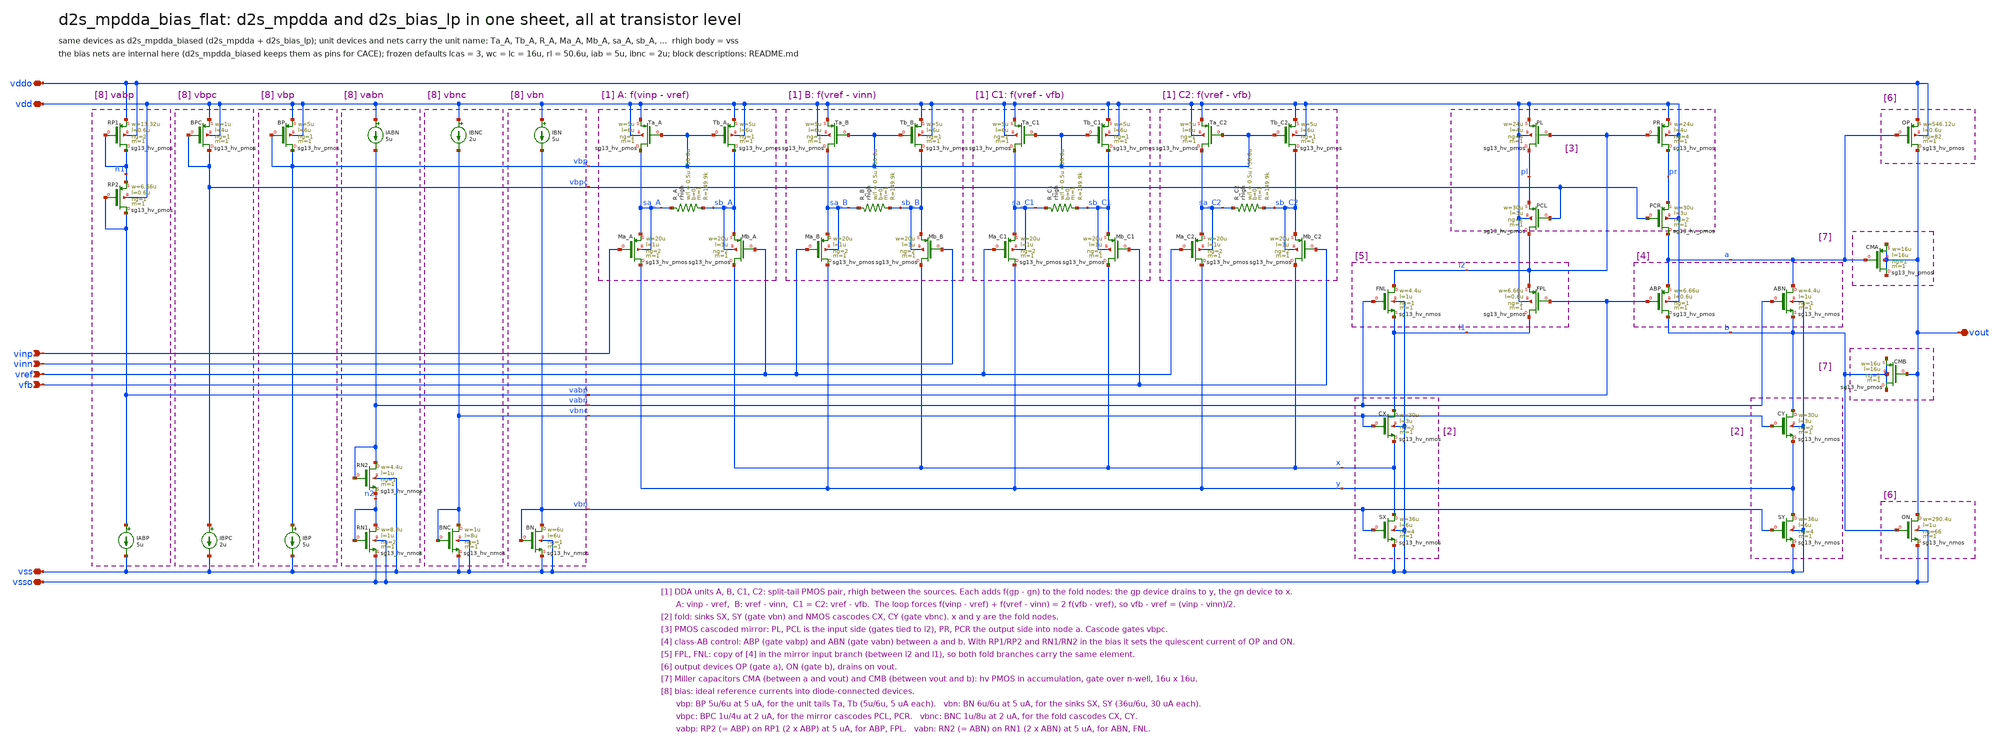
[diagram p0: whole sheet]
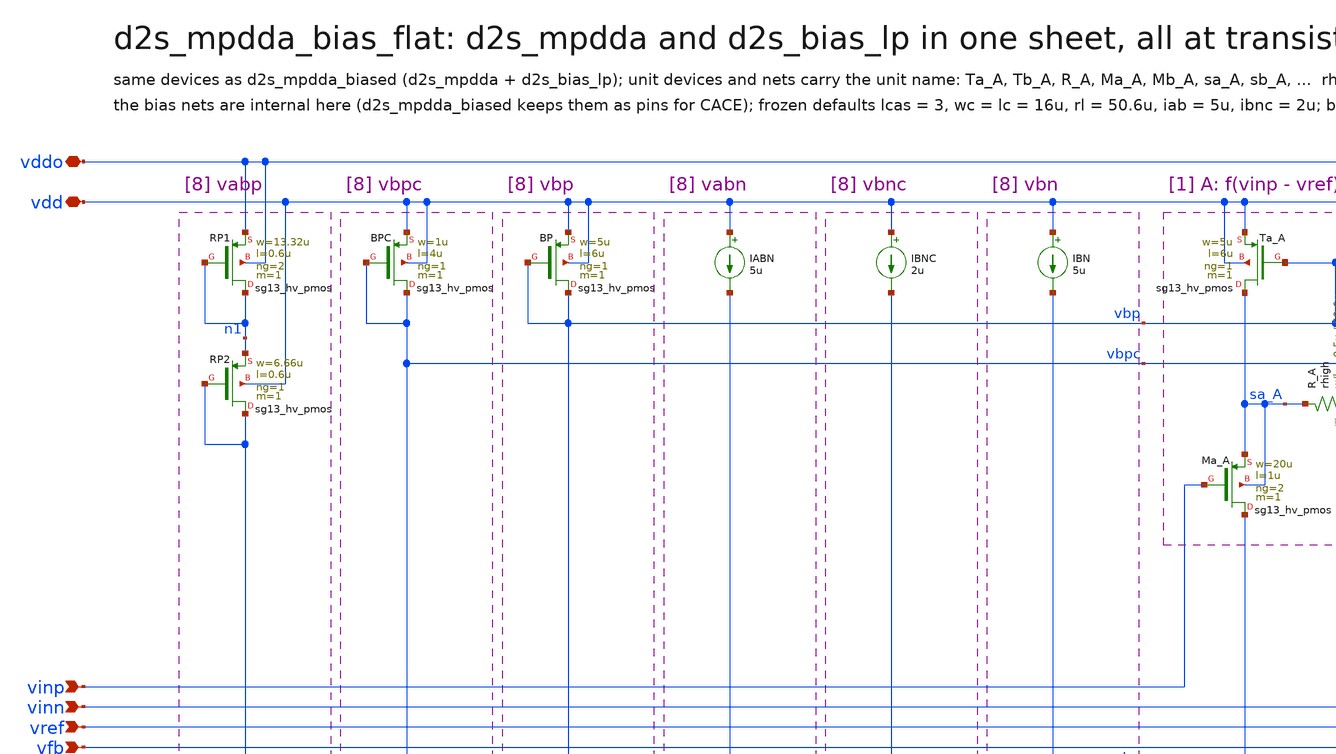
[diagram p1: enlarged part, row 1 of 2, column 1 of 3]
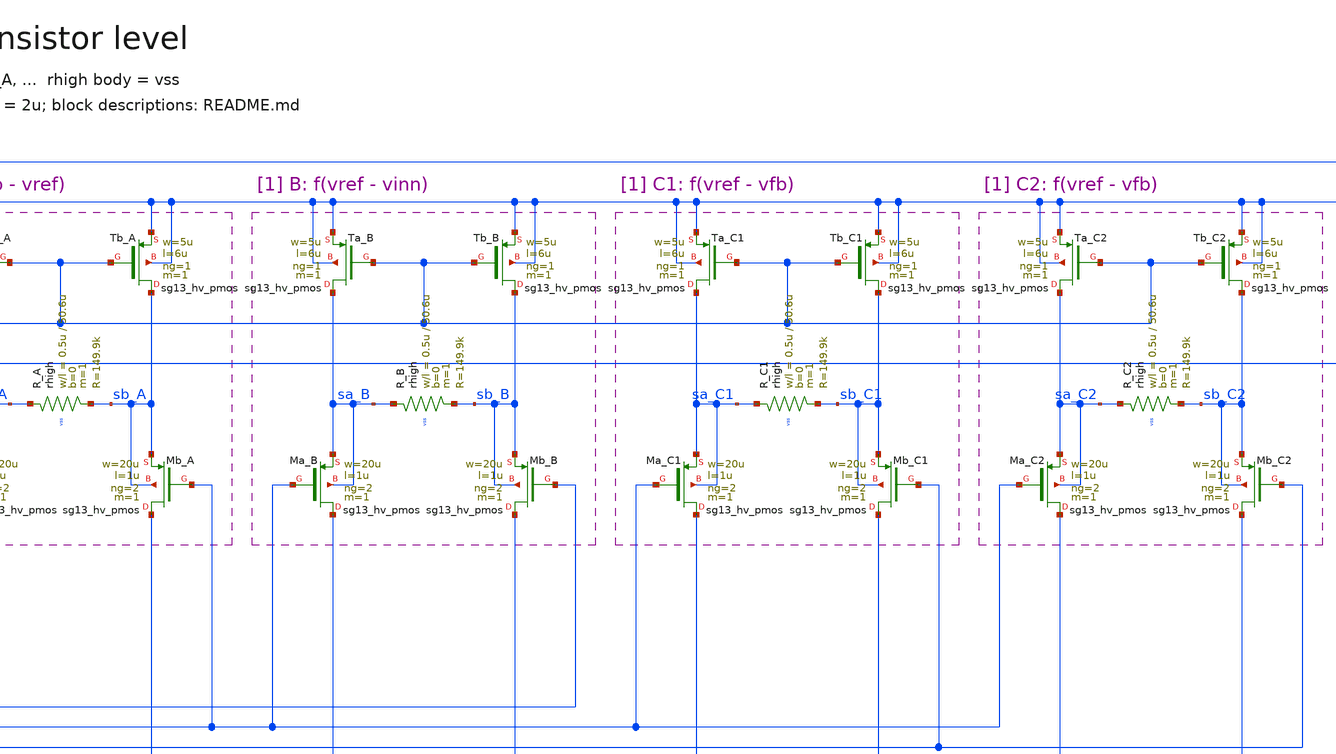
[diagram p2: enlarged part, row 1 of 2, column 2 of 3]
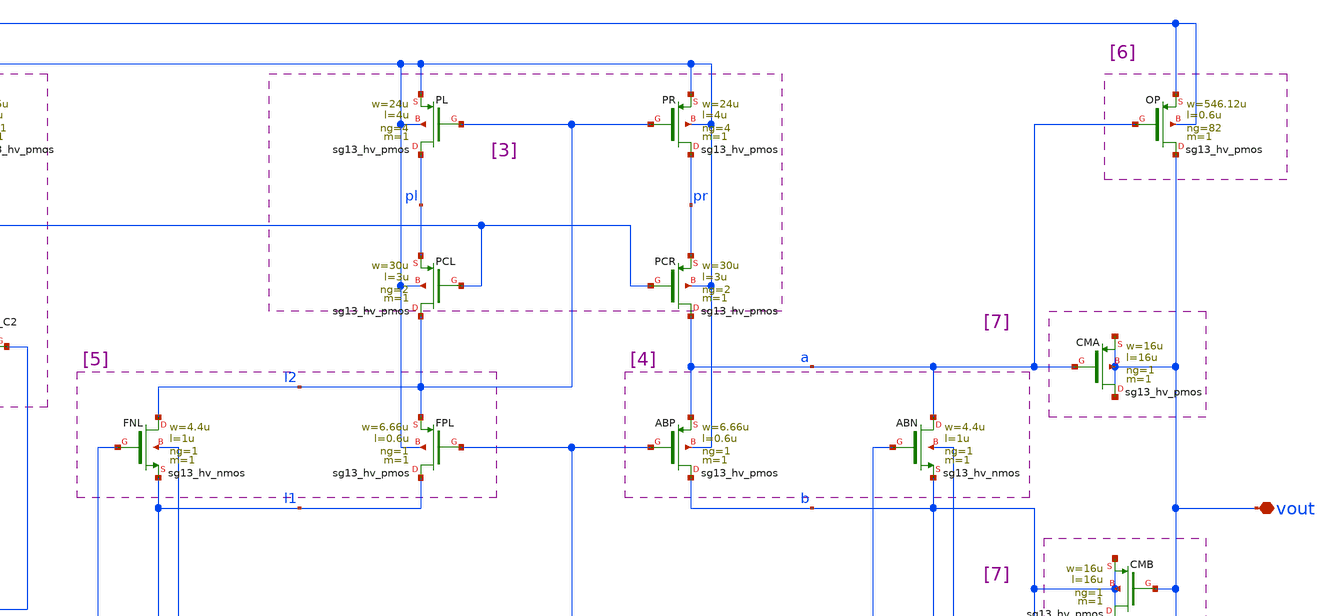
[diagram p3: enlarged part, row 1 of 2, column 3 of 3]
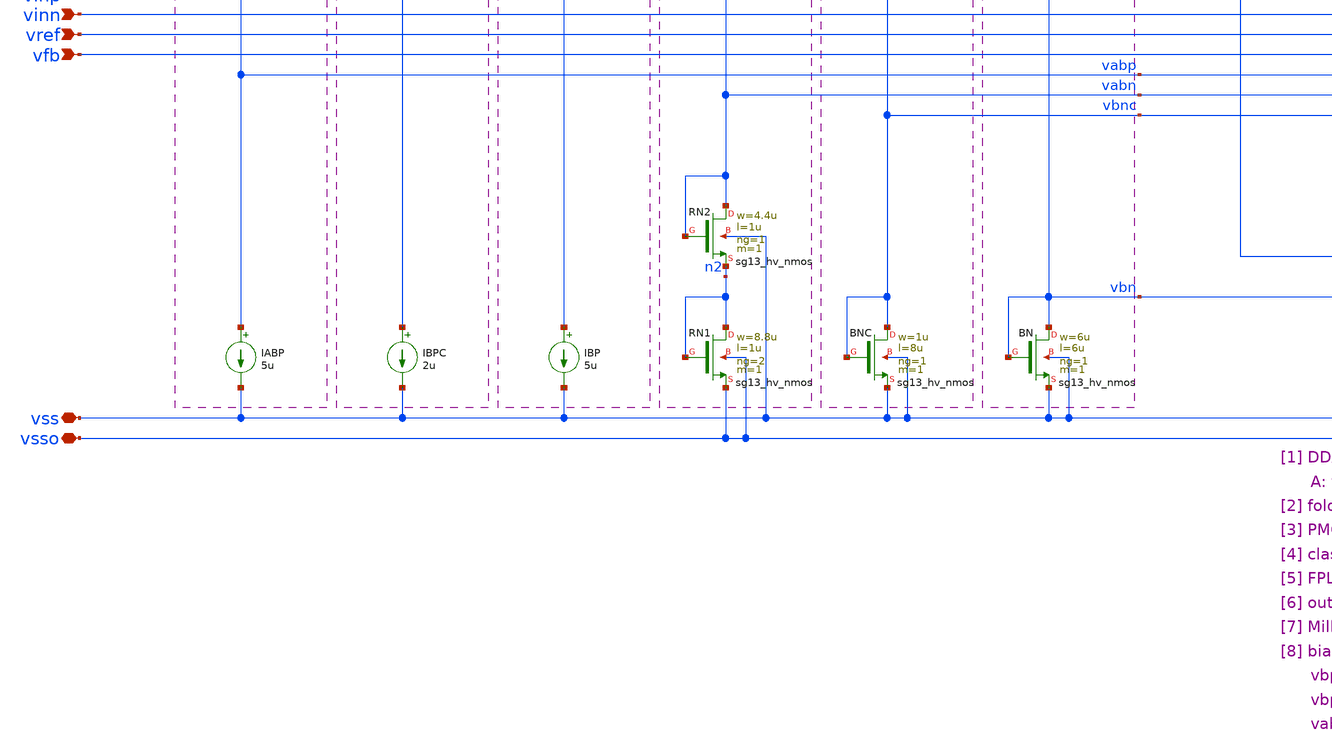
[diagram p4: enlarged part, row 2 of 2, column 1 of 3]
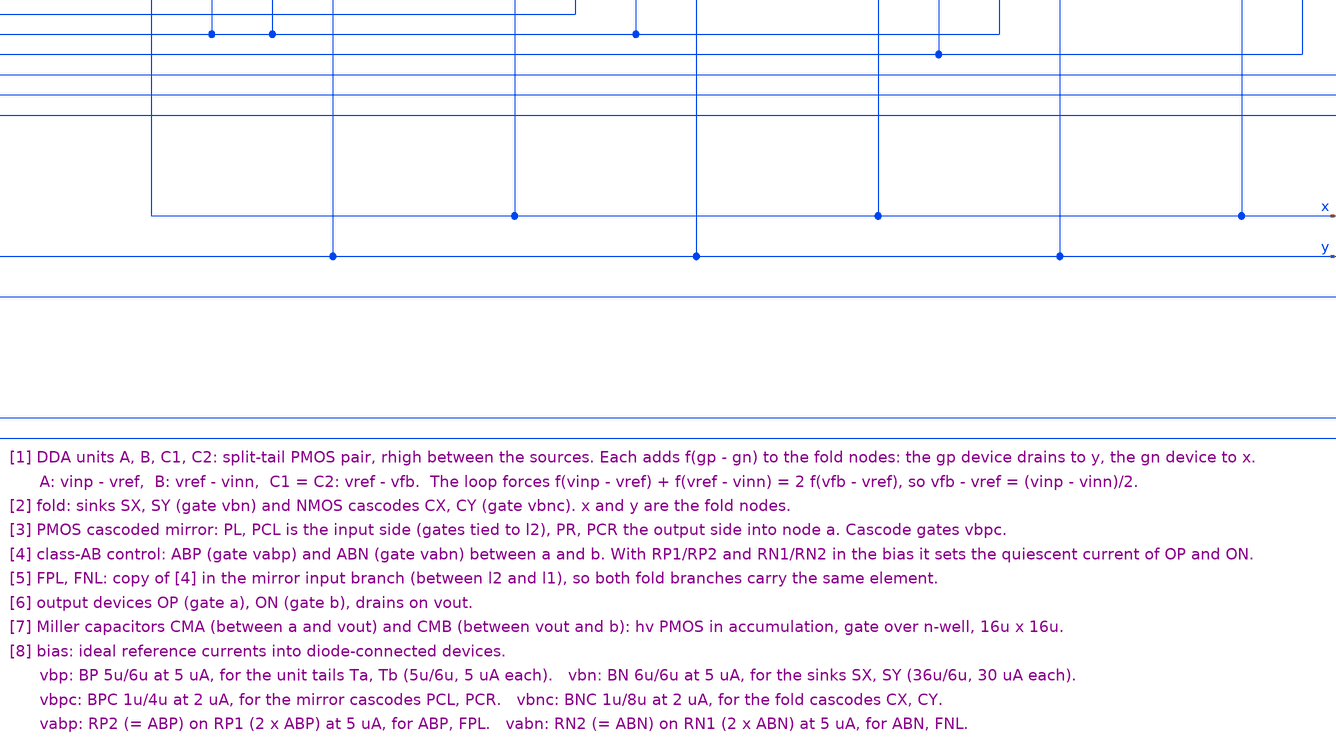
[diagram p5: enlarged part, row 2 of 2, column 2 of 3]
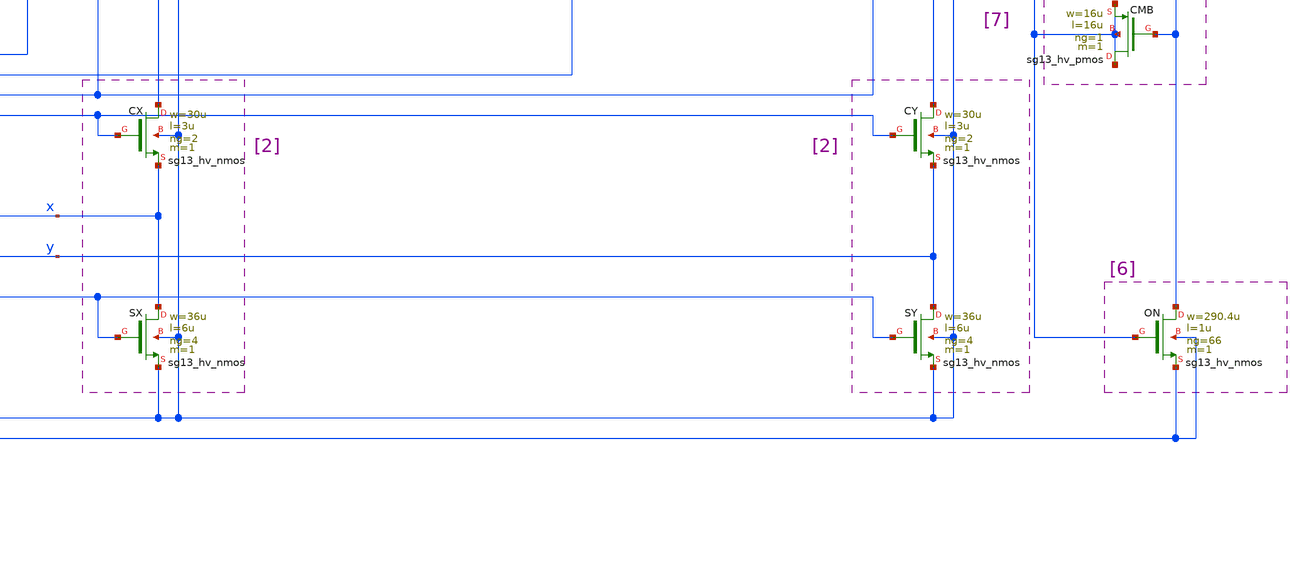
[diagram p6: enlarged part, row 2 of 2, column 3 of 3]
** sch_path: sudelbuecher/design_considerations/class_ab_pad_driver/improvements/xschem/d2s_mpdda_bias_flat.sch
**.subckt d2s_mpdda_bias_flat vdd vss vddo vsso vinp vinn vref vout vfb
*.iopin vdd
*.iopin vss
*.iopin vddo
*.iopin vsso
*.ipin vinp
*.ipin vinn
*.ipin vref
*.iopin vout
*.ipin vfb
XRP1 n1 n1 vddo vddo sg13_hv_pmos w=13.32u l=0.6u ng=2 m=1 mm_ok=1
XRP2 vabp vabp n1 vdd sg13_hv_pmos w=6.66u l=0.6u ng=1 m=1 mm_ok=1
IABP vabp vss 5u
XBPC vbpc vbpc vdd vdd sg13_hv_pmos w=1u l=4u ng=1 m=1 mm_ok=1
IBPC vbpc vss 2u
XBP vbp vbp vdd vdd sg13_hv_pmos w=5u l=6u ng=1 m=1 mm_ok=1
IBP vbp vss 5u
IABN vdd vabn 5u
XRN2 vabn vabn n2 vss sg13_hv_nmos w=4.4u l=1u ng=1 m=1 mm_ok=1
XRN1 n2 n2 vsso vsso sg13_hv_nmos w=8.8u l=1u ng=2 m=1 mm_ok=1
IBNC vdd vbnc 2u
XBNC vbnc vbnc vss vss sg13_hv_nmos w=1u l=8u ng=1 m=1 mm_ok=1
IBN vdd vbn 5u
XBN vbn vbn vss vss sg13_hv_nmos w=6u l=6u ng=1 m=1 mm_ok=1
XTa_A sa_A vbp vdd vdd sg13_hv_pmos w=5u l=6u ng=1 m=1 mm_ok=1
XTb_A sb_A vbp vdd vdd sg13_hv_pmos w=5u l=6u ng=1 m=1 mm_ok=1
XR_A sa_A sb_A vss rhigh w=0.5u l=50.6u m=1 b=0 mm_ok=1
XMa_A y vinp sa_A sa_A sg13_hv_pmos w=20u l=1u ng=2 m=1 mm_ok=1
XMb_A x vref sb_A sb_A sg13_hv_pmos w=20u l=1u ng=2 m=1 mm_ok=1
XTa_B sa_B vbp vdd vdd sg13_hv_pmos w=5u l=6u ng=1 m=1 mm_ok=1
XTb_B sb_B vbp vdd vdd sg13_hv_pmos w=5u l=6u ng=1 m=1 mm_ok=1
XR_B sa_B sb_B vss rhigh w=0.5u l=50.6u m=1 b=0 mm_ok=1
XMa_B y vref sa_B sa_B sg13_hv_pmos w=20u l=1u ng=2 m=1 mm_ok=1
XMb_B x vinn sb_B sb_B sg13_hv_pmos w=20u l=1u ng=2 m=1 mm_ok=1
XTa_C1 sa_C1 vbp vdd vdd sg13_hv_pmos w=5u l=6u ng=1 m=1 mm_ok=1
XTb_C1 sb_C1 vbp vdd vdd sg13_hv_pmos w=5u l=6u ng=1 m=1 mm_ok=1
XR_C1 sa_C1 sb_C1 vss rhigh w=0.5u l=50.6u m=1 b=0 mm_ok=1
XMa_C1 y vref sa_C1 sa_C1 sg13_hv_pmos w=20u l=1u ng=2 m=1 mm_ok=1
XMb_C1 x vfb sb_C1 sb_C1 sg13_hv_pmos w=20u l=1u ng=2 m=1 mm_ok=1
XTa_C2 sa_C2 vbp vdd vdd sg13_hv_pmos w=5u l=6u ng=1 m=1 mm_ok=1
XTb_C2 sb_C2 vbp vdd vdd sg13_hv_pmos w=5u l=6u ng=1 m=1 mm_ok=1
XR_C2 sa_C2 sb_C2 vss rhigh w=0.5u l=50.6u m=1 b=0 mm_ok=1
XMa_C2 y vref sa_C2 sa_C2 sg13_hv_pmos w=20u l=1u ng=2 m=1 mm_ok=1
XMb_C2 x vfb sb_C2 sb_C2 sg13_hv_pmos w=20u l=1u ng=2 m=1 mm_ok=1
XFNL l2 vabn l1 vss sg13_hv_nmos w=4.4u l=1u ng=1 m=1 mm_ok=1
XCX l1 vbnc x vss sg13_hv_nmos w=30u l=3u ng=2 m=1 mm_ok=1
XSX x vbn vss vss sg13_hv_nmos w=36u l=6u ng=4 m=1 mm_ok=1
XPL pl l2 vdd vdd sg13_hv_pmos w=24u l=4u ng=4 m=1 mm_ok=1
XPCL l2 vbpc pl vdd sg13_hv_pmos w=30u l=3u ng=2 m=1 mm_ok=1
XFPL l1 vabp l2 vdd sg13_hv_pmos w=6.66u l=0.6u ng=1 m=1 mm_ok=1
XPR pr l2 vdd vdd sg13_hv_pmos w=24u l=4u ng=4 m=1 mm_ok=1
XPCR a vbpc pr vdd sg13_hv_pmos w=30u l=3u ng=2 m=1 mm_ok=1
XABP b vabp a vdd sg13_hv_pmos w=6.66u l=0.6u ng=1 m=1 mm_ok=1
XABN a vabn b vss sg13_hv_nmos w=4.4u l=1u ng=1 m=1 mm_ok=1
XCY b vbnc y vss sg13_hv_nmos w=30u l=3u ng=2 m=1 mm_ok=1
XSY y vbn vss vss sg13_hv_nmos w=36u l=6u ng=4 m=1 mm_ok=1
XOP vout a vddo vddo sg13_hv_pmos w=546.12u l=0.6u ng=82 m=1 mm_ok=1
XON vout b vsso vsso sg13_hv_nmos w=290.4u l=1u ng=66 m=1 mm_ok=1
XCMA vout a vout vout sg13_hv_pmos w=16u l=16u ng=1 m=1 mm_ok=1
XCMB b vout b b sg13_hv_pmos w=16u l=16u ng=1 m=1 mm_ok=1
**.ends
.end
